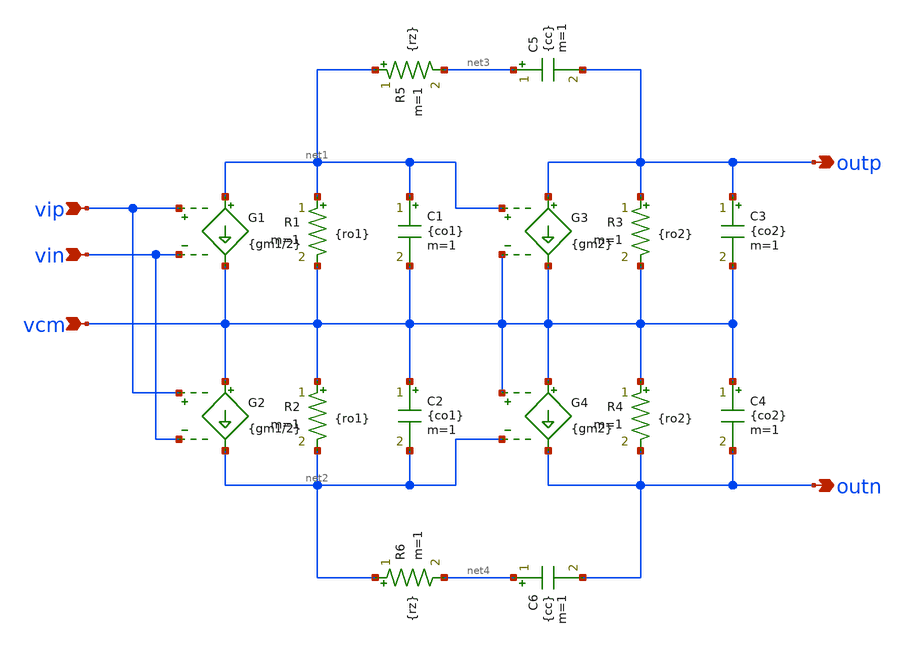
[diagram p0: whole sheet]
** sch_path: modules/ideal_op_diff_2stage.sch
**.subckt ideal_op_diff_2stage vip vin outp outn vcm
*.ipin vip
*.ipin vin
*.opin outp
*.opin outn
*.ipin vcm
G1 net1 vcm vip vin {gm1/2}
G2 vcm net2 vip vin {gm1/2}
R1 net1 vcm {ro1} m=1
R2 vcm net2 {ro1} m=1
C1 net1 vcm {co1} m=1
C2 vcm net2 {co1} m=1
G3 outp vcm net1 vcm {gm2}
G4 vcm outn vcm net2 {gm2}
R3 outp vcm {ro2} m=1
R4 vcm outn {ro2} m=1
C3 outp vcm {co2} m=1
C4 vcm outn {co2} m=1
R5 net1 net3 {rz} m=1
C5 net3 outp {cc} m=1
R6 net2 net4 {rz} m=1
C6 net4 outn {cc} m=1
**.ends
.end
